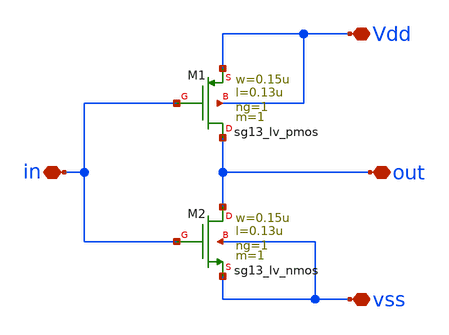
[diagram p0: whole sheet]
** sch_path: design/blocks/inversor/schematic/inversor.sch
**.subckt inversor Vdd out vss in
*.iopin Vdd
*.iopin out
*.iopin vss
*.iopin in
XM1 out in Vdd Vdd sg13_lv_pmos w=0.15u l=0.13u ng=1 m=1 mm_ok=1
XM2 out in vss vss sg13_lv_nmos w=0.15u l=0.13u ng=1 m=1 mm_ok=1
**.ends
.end
